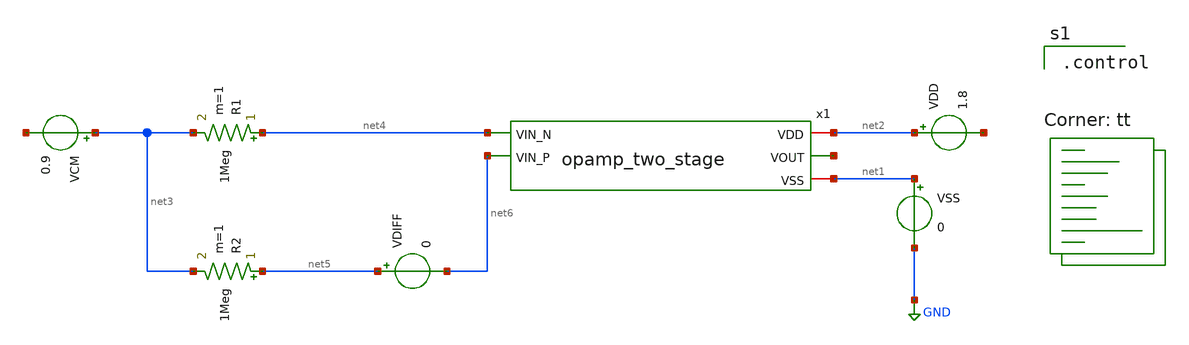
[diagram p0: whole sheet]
** sch_path: analog/build/schematic/tb_dc_analysis.sch
**.subckt tb_dc_analysis
x1 net2 net4 net6 net7 net1 opamp_two_stage
VDD net2 net8 1.8
VSS net1 GND 0
VCM net3 net9 0.9
R1 net4 net3 1Meg m=1
R2 net5 net3 1Meg m=1
VDIFF net5 net6 0
**** begin user architecture code

.control

.lib $::SKYWATER_MODELS/sky130.lib.spice tt
**** end user architecture code
**.ends
.GLOBAL GND
.end
